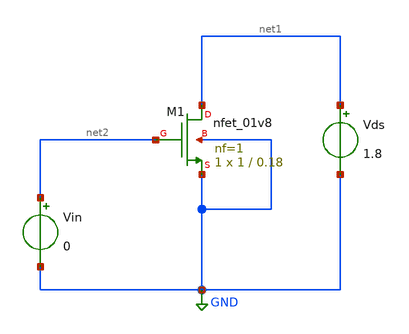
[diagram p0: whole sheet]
** sch_path: projects/tutorial/xschem_ngspice/tutorial.sch
**.subckt tutorial
XM1 net1 net2 GND GND sky130_fd_pr__nfet_01v8 L=0.18 W=1 nf=1 ad='int((nf+1)/2) * W/nf * 0.29' as='int((nf+2)/2) * W/nf * 0.29'
+ pd='2*int((nf+1)/2) * (W/nf + 0.29)' ps='2*int((nf+2)/2) * (W/nf + 0.29)' nrd='0.29 / W' nrs='0.29 / W'
+ sa=0 sb=0 sd=0 mult=1 m=1
Vin net2 GND 0
Vds net1 GND 1.8
**** begin user architecture code




.lib /foss/pdks/sky130A/libs.tech/ngspice/sky130.lib.spice tt


.control
    * dc Vds 0 3 0.01 Vin 0 5 1
    dc Vin 0 5 0.01
    * Calculate and plot gm
    let gm = deriv(-i(Vds), v(net2))
    plot gm ylimit 0 0.0006
    plot -i(Vds)

.endc


.save all





**** end user architecture code
**.ends
.GLOBAL GND
.end
